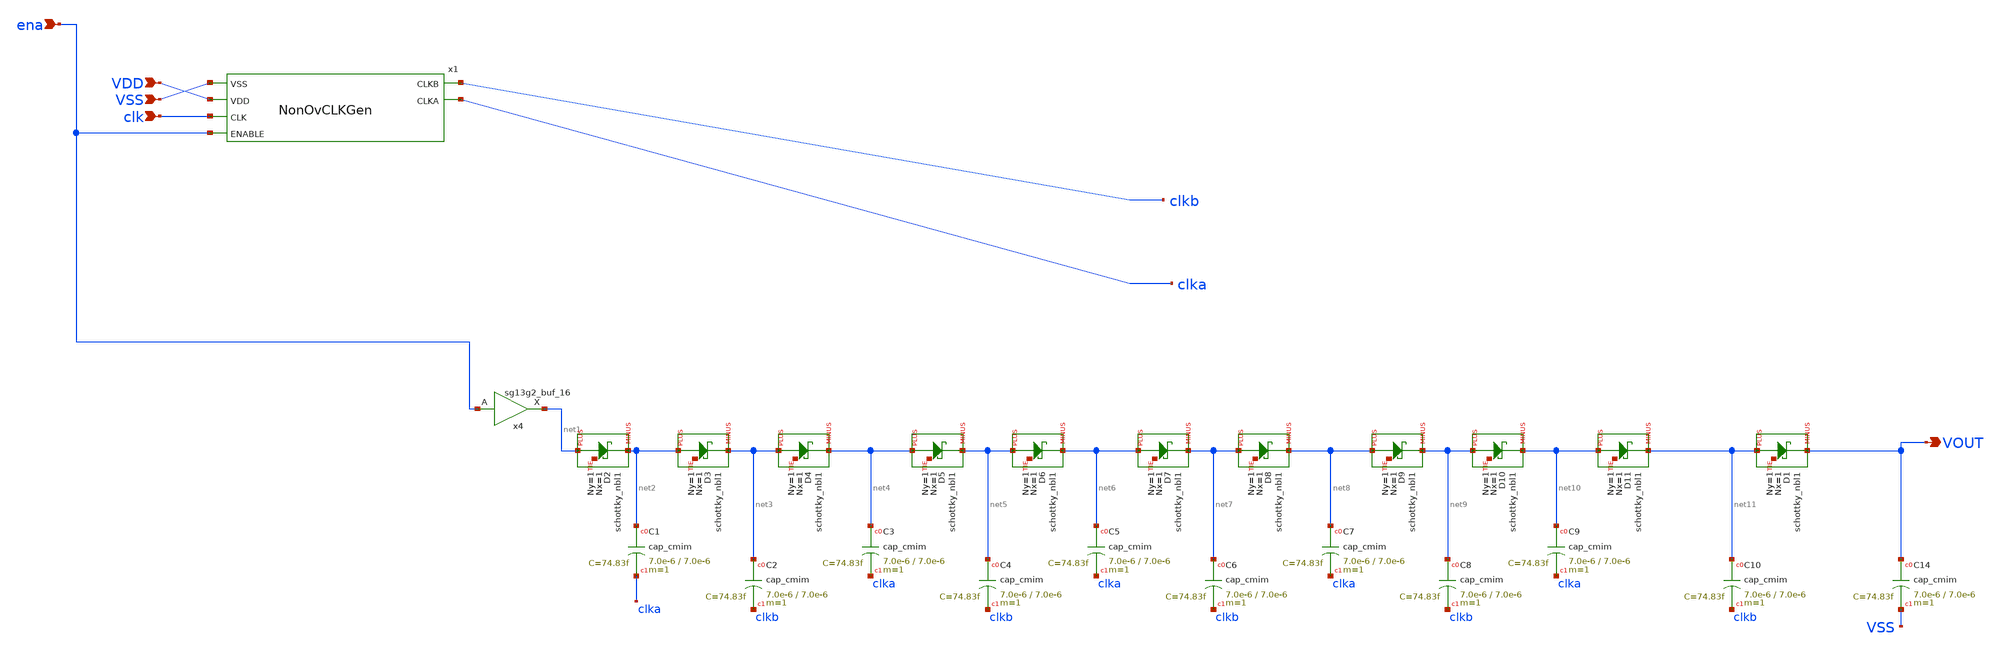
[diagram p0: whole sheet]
** sch_path: ihp130_cells/Schottky_PosChargePump/schottky_pump.sch
* IHP-GmbH/IHP-Open-PDK/ihp-sg13g2/libs.tech/xschem/sg13g2_stdcells/sg13g2_inv_2.sch:
* Copyright 2023 IHP PDK Authors
* Licensed under the Apache License, Version 2.0 (the "License");
**.subckt schottky_pump ena VDD VSS VOUT clk
*.ipin ena
*.ipin VDD
*.ipin VSS
*.opin VOUT
*.ipin clk
XC1 net2 clka cap_cmim w=7.0e-6 l=7.0e-6 m=1 mm_ok=1
x4 net1 ena VDD VSS sg13g2_buf_16
XD2 net1 net2 net12 schottky_nbl1 Nx=1 Ny=1
XD3 net2 net3 net13 schottky_nbl1 Nx=1 Ny=1
XD4 net3 net4 net14 schottky_nbl1 Nx=1 Ny=1
XD5 net4 net5 net15 schottky_nbl1 Nx=1 Ny=1
XD6 net5 net6 net16 schottky_nbl1 Nx=1 Ny=1
XD7 net6 net7 net17 schottky_nbl1 Nx=1 Ny=1
XD8 net7 net8 net18 schottky_nbl1 Nx=1 Ny=1
XD9 net8 net9 net19 schottky_nbl1 Nx=1 Ny=1
XD10 net9 net10 net20 schottky_nbl1 Nx=1 Ny=1
XD11 net10 net11 net21 schottky_nbl1 Nx=1 Ny=1
XC2 net3 clkb cap_cmim w=7.0e-6 l=7.0e-6 m=1 mm_ok=1
XC3 net4 clka cap_cmim w=7.0e-6 l=7.0e-6 m=1 mm_ok=1
XC4 net5 clkb cap_cmim w=7.0e-6 l=7.0e-6 m=1 mm_ok=1
XC5 net6 clka cap_cmim w=7.0e-6 l=7.0e-6 m=1 mm_ok=1
XC6 net7 clkb cap_cmim w=7.0e-6 l=7.0e-6 m=1 mm_ok=1
XC7 net8 clka cap_cmim w=7.0e-6 l=7.0e-6 m=1 mm_ok=1
XC8 net9 clkb cap_cmim w=7.0e-6 l=7.0e-6 m=1 mm_ok=1
XC9 net10 clka cap_cmim w=7.0e-6 l=7.0e-6 m=1 mm_ok=1
XC14 VOUT VSS cap_cmim w=7.0e-6 l=7.0e-6 m=1 mm_ok=1
XD1 net11 VOUT net22 schottky_nbl1 Nx=1 Ny=1
XC10 net11 clkb cap_cmim w=7.0e-6 l=7.0e-6 m=1 mm_ok=1
x1 VSS VDD clk clkb clka ena NonOvCLKGen
**.ends

* expanding   symbol:  sg13g2_stdcells/sg13g2_buf_16.sym # of pins=2
** sym_path: sg13g2_stdcells/sg13g2_buf_16.sym
** sch_path: sg13g2_stdcells/sg13g2_buf_16.sch
.subckt sg13g2_buf_16 X A VDD VSS
*.ipin A
*.opin X
*.iopin VDD
*.iopin VSS
XM1 net1 A VSS VSS sg13_lv_nmos w=4.44u l=130.00n ng=6 m=1 mm_ok=1
XM2 X net1 VSS VSS sg13_lv_nmos w=11.84u l=130.00n ng=16 m=1 mm_ok=1
XM3 net1 A VDD VDD sg13_lv_pmos w=6.72u l=130.00n ng=6 m=1 mm_ok=1
XM4 X net1 VDD VDD sg13_lv_pmos w=17.92u l=130.00n ng=16 m=1 mm_ok=1
.ends


* expanding   symbol:  NonOvCLKGen/NonOvCLKGen.sym # of pins=6
** sym_path: ihp130_cells/NonOvCLKGen/NonOvCLKGen.sym
** sch_path: ihp130_cells/NonOvCLKGen/NonOvCLKGen.sch
.subckt NonOvCLKGen VSS VDD CLK CLKB CLKA ENABLE
*.ipin CLK
*.ipin ENABLE
*.opin CLKB
*.opin CLKA
*.ipin VDD
*.ipin VSS
x1 CLKA net4 ENABLE VDD VSS sg13g2_and2_2
x3 CLKB net3 ENABLE VDD VSS sg13g2_and2_2
x5 net1 net7 net4 VDD VSS sg13g2_nor2_2
x6 net5 net3 CLK VDD VSS sg13g2_nor2_2
x7 net7 CLK VDD VSS sg13g2_inv_2
x8 net2 net1 VDD VSS sg13g2_inv_2
x2 net6 net5 VDD VSS sg13g2_inv_2
x4 net4 net6 VDD VSS sg13g2_inv_2
x9 net3 net2 VDD VSS sg13g2_inv_2
.ends


* expanding   symbol:  sg13g2_stdcells/sg13g2_and2_2.sym # of pins=3
** sym_path: sg13g2_stdcells/sg13g2_and2_2.sym
** sch_path: sg13g2_stdcells/sg13g2_and2_2.sch
.subckt sg13g2_and2_2 X A B VDD VSS
*.ipin A
*.ipin B
*.opin X
*.iopin VDD
*.iopin VSS
XM1 net1 A net2 VSS sg13_lv_nmos w=640.00n l=130.00n ng=1 m=1 mm_ok=1
XM2 net2 B VSS VSS sg13_lv_nmos w=640.00n l=130.00n ng=1 m=1 mm_ok=1
XM3 X net1 VSS VSS sg13_lv_nmos w=1.48u l=130.00n ng=2 m=1 mm_ok=1
XM4 net1 B VDD VDD sg13_lv_pmos w=840.00n l=130.00n ng=1 m=1 mm_ok=1
XM5 net1 A VDD VDD sg13_lv_pmos w=840.00n l=130.00n ng=1 m=1 mm_ok=1
XM6 X net1 VDD VDD sg13_lv_pmos w=2.24u l=130.00n ng=2 m=1 mm_ok=1
.ends


* expanding   symbol:
*+  /srv/cadsp/pdks/open_pdks/IHP-Open-PDK/ihp-sg13g2/libs.tech/xschem/sg13g2_stdcells/sg13g2_nor2_2.sym # of pins=3
** sym_path: /srv/cadsp/pdks/open_pdks/IHP-Open-PDK/ihp-sg13g2/libs.tech/xschem/sg13g2_stdcells/sg13g2_nor2_2.sym
** sch_path: /srv/cadsp/pdks/open_pdks/IHP-Open-PDK/ihp-sg13g2/libs.tech/xschem/sg13g2_stdcells/sg13g2_nor2_2.sch
.subckt sg13g2_nor2_2 Y A B VDD VSS
*.opin Y
*.ipin B
*.ipin A
*.iopin VDD
*.iopin VSS
XM1 Y A VSS VSS sg13_lv_nmos w=1.48u l=130.00n ng=2 m=1 mm_ok=1
XM2 Y B VSS VSS sg13_lv_nmos w=1.48u l=130.00n ng=2 m=1 mm_ok=1
XM3 net1 A VDD VDD sg13_lv_pmos w=2.24u l=130.00n ng=2 m=1 mm_ok=1
XM4 Y B net1 VDD sg13_lv_pmos w=2.24u l=130.00n ng=2 m=1 mm_ok=1
.ends


* expanding   symbol:  sg13g2_stdcells/sg13g2_inv_2.sym # of pins=2
** sym_path: sg13g2_stdcells/sg13g2_inv_2.sym
** sch_path: sg13g2_stdcells/sg13g2_inv_2.sch
.subckt sg13g2_inv_2 Y A VDD VSS
*.opin Y
*.ipin A
*.iopin VDD
*.iopin VSS
XM1 Y A VSS VSS sg13_lv_nmos w=1.48u l=130.00n ng=2 m=1 mm_ok=1
XM2 Y A VDD VDD sg13_lv_pmos w=2.24u l=130.00n ng=2 m=1 mm_ok=1
.ends

.end
